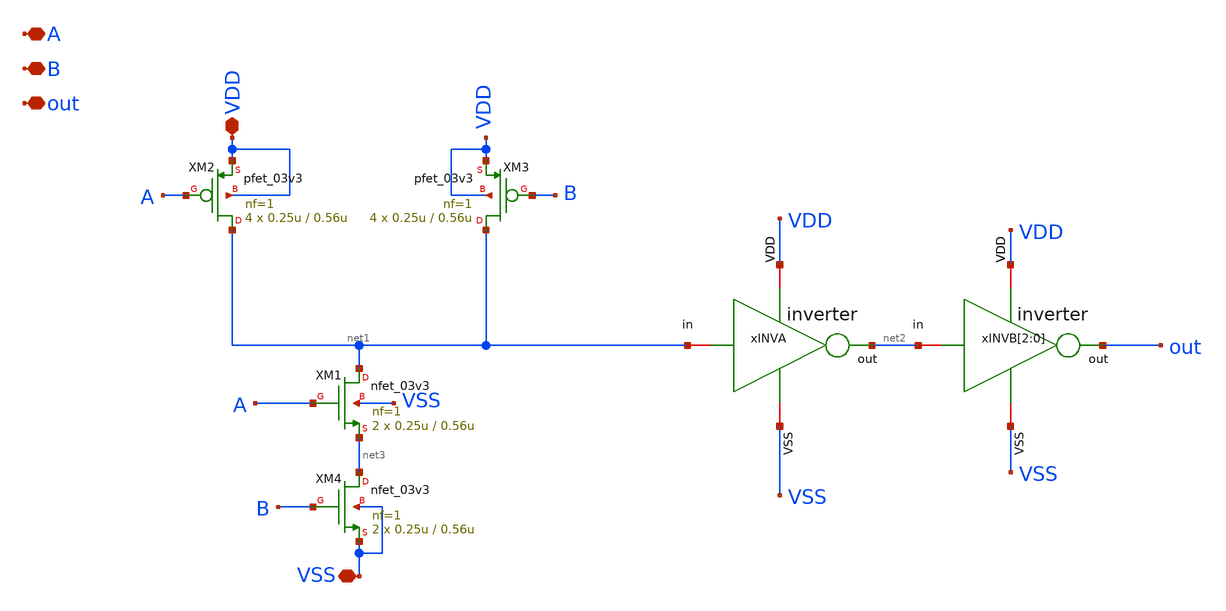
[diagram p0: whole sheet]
** sch_path: designs/sar_adc/digital/nand_edge/xschem/NAND.sch
**.subckt NAND VDD A B out VSS
*.iopin VDD
*.iopin A
*.iopin B
*.iopin out
*.iopin VSS
xINVA VDD net1 net2 VSS inverter
xINVB[2] VDD net2 out VSS inverter
xINVB[1] VDD net2 out VSS inverter
xINVB[0] VDD net2 out VSS inverter
XM2 net1 A VDD VDD pfet_03v3 L=0.56u W=0.25u nf=1 ad='int((nf+1)/2) * W/nf * 0.18u' as='int((nf+2)/2) * W/nf * 0.18u'
+ pd='2*int((nf+1)/2) * (W/nf + 0.18u)' ps='2*int((nf+2)/2) * (W/nf + 0.18u)' nrd='0.18u / W' nrs='0.18u / W'
+ sa=0 sb=0 sd=0 m=4
XM1 net1 A net3 VSS nfet_03v3 L=0.56u W=0.25u nf=1 ad='int((nf+1)/2) * W/nf * 0.18u' as='int((nf+2)/2) * W/nf * 0.18u'
+ pd='2*int((nf+1)/2) * (W/nf + 0.18u)' ps='2*int((nf+2)/2) * (W/nf + 0.18u)' nrd='0.18u / W' nrs='0.18u / W'
+ sa=0 sb=0 sd=0 m=2
XM3 net1 B VDD VDD pfet_03v3 L=0.56u W=0.25u nf=1 ad='int((nf+1)/2) * W/nf * 0.18u' as='int((nf+2)/2) * W/nf * 0.18u'
+ pd='2*int((nf+1)/2) * (W/nf + 0.18u)' ps='2*int((nf+2)/2) * (W/nf + 0.18u)' nrd='0.18u / W' nrs='0.18u / W'
+ sa=0 sb=0 sd=0 m=4
XM4 net3 B VSS VSS nfet_03v3 L=0.56u W=0.25u nf=1 ad='int((nf+1)/2) * W/nf * 0.18u' as='int((nf+2)/2) * W/nf * 0.18u'
+ pd='2*int((nf+1)/2) * (W/nf + 0.18u)' ps='2*int((nf+2)/2) * (W/nf + 0.18u)' nrd='0.18u / W' nrs='0.18u / W'
+ sa=0 sb=0 sd=0 m=2
**.ends

* expanding   symbol:  designs/sar_adc/digital/inverter/xschem/inverter.sym # of pins=6
** sym_path: designs/sar_adc/digital/inverter/xschem/inverter.sym
** sch_path: designs/sar_adc/digital/inverter/xschem/inverter.sch
.subckt inverter VDD in out VSS
*.opin out
*.iopin in
*.iopin VDD
*.iopin VSS
XM1 out in VSS VSS nfet_03v3 L=0.28u W=1u nf=1 ad='int((nf+1)/2) * W/nf * 0.18u' as='int((nf+2)/2) * W/nf * 0.18u'
+ pd='2*int((nf+1)/2) * (W/nf + 0.18u)' ps='2*int((nf+2)/2) * (W/nf + 0.18u)' nrd='0.18u / W' nrs='0.18u / W'
+ sa=0 sb=0 sd=0 m=1
XM2 out in VDD VDD pfet_03v3 L=0.28u W=3u nf=1 ad='int((nf+1)/2) * W/nf * 0.18u' as='int((nf+2)/2) * W/nf * 0.18u'
+ pd='2*int((nf+1)/2) * (W/nf + 0.18u)' ps='2*int((nf+2)/2) * (W/nf + 0.18u)' nrd='0.18u / W' nrs='0.18u / W'
+ sa=0 sb=0 sd=0 m=1
.ends

.end
